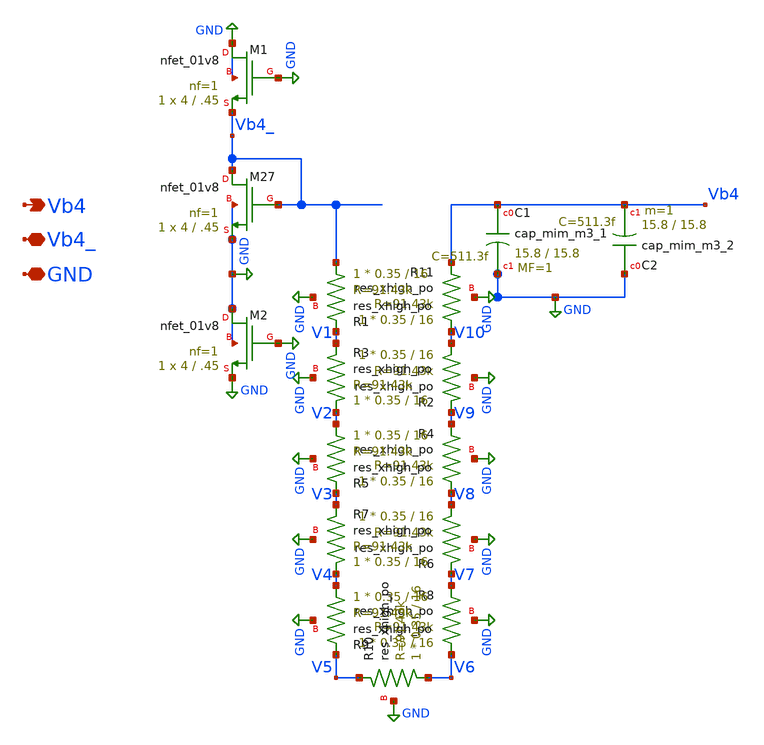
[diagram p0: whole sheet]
** sch_path: xschem/mirror_4.sch
**.subckt mirror_4 GND Vb4_ Vb4
*.iopin GND
*.iopin Vb4_
*.opin Vb4
XM27 Vb4_ Vb4_ GND GND sky130_fd_pr__nfet_01v8 L=.45 W=4 nf=1 ad='int((nf+1)/2) * W/nf * 0.29' as='int((nf+2)/2) * W/nf * 0.29'
+ pd='2*int((nf+1)/2) * (W/nf + 0.29)' ps='2*int((nf+2)/2) * (W/nf + 0.29)' nrd='0.29 / W' nrs='0.29 / W'
+ sa=0 sb=0 sd=0 mult=1 m=1
XC1 Vb4 GND sky130_fd_pr__cap_mim_m3_1 W=15.8 L=15.8 MF=1 m=1
XC2 GND Vb4 sky130_fd_pr__cap_mim_m3_2 W=15.8 L=15.8 MF=1 m=1
XR11 V10 Vb4 GND sky130_fd_pr__res_xhigh_po W=0.35 L=16 mult=1 m=1
XR1 Vb4_ V1 GND sky130_fd_pr__res_xhigh_po W=0.35 L=16 mult=1 m=1
XR2 V10 V9 GND sky130_fd_pr__res_xhigh_po W=0.35 L=16 mult=1 m=1
XR3 V2 V1 GND sky130_fd_pr__res_xhigh_po W=0.35 L=16 mult=1 m=1
XR4 V8 V9 GND sky130_fd_pr__res_xhigh_po W=0.35 L=16 mult=1 m=1
XR5 V2 V3 GND sky130_fd_pr__res_xhigh_po W=0.35 L=16 mult=1 m=1
XR6 V8 V7 GND sky130_fd_pr__res_xhigh_po W=0.35 L=16 mult=1 m=1
XR7 V4 V3 GND sky130_fd_pr__res_xhigh_po W=0.35 L=16 mult=1 m=1
XR8 V6 V7 GND sky130_fd_pr__res_xhigh_po W=0.35 L=16 mult=1 m=1
XR9 V4 V5 GND sky130_fd_pr__res_xhigh_po W=0.35 L=16 mult=1 m=1
XR10 V6 V5 GND sky130_fd_pr__res_xhigh_po W=0.35 L=16 mult=1 m=1
XM1 GND GND Vb4_ GND sky130_fd_pr__nfet_01v8 L=.45 W=4 nf=1 ad='int((nf+1)/2) * W/nf * 0.29' as='int((nf+2)/2) * W/nf * 0.29'
+ pd='2*int((nf+1)/2) * (W/nf + 0.29)' ps='2*int((nf+2)/2) * (W/nf + 0.29)' nrd='0.29 / W' nrs='0.29 / W'
+ sa=0 sb=0 sd=0 mult=1 m=1
XM2 GND GND GND GND sky130_fd_pr__nfet_01v8 L=.45 W=4 nf=1 ad='int((nf+1)/2) * W/nf * 0.29' as='int((nf+2)/2) * W/nf * 0.29'
+ pd='2*int((nf+1)/2) * (W/nf + 0.29)' ps='2*int((nf+2)/2) * (W/nf + 0.29)' nrd='0.29 / W' nrs='0.29 / W'
+ sa=0 sb=0 sd=0 mult=1 m=1
**.ends
.GLOBAL GND
.end
